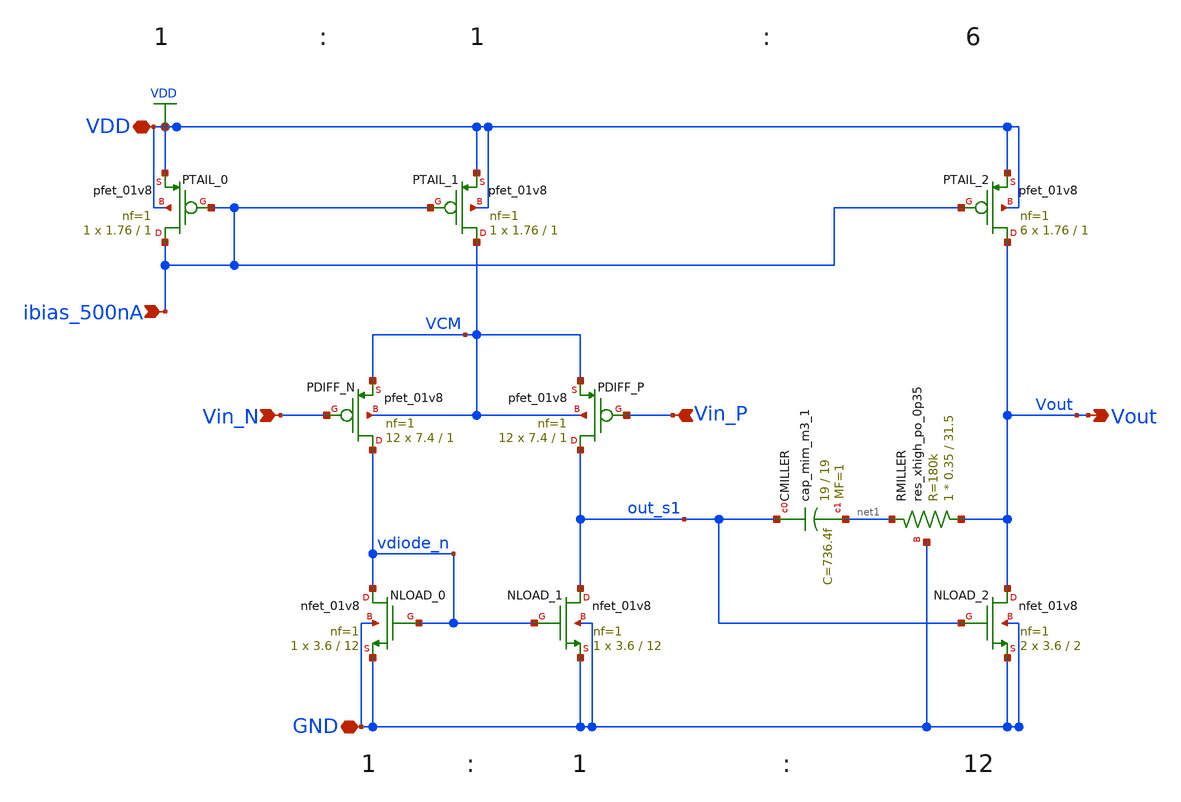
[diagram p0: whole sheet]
** sch_path: dfii/project_2stage_OTA/ota_2stage_transistor.sch
**.subckt ota_2stage_transistor VDD GND ibias_500nA Vin_N Vin_P Vout
*.iopin VDD
*.iopin GND
*.ipin ibias_500nA
*.ipin Vin_N
*.ipin Vin_P
*.opin Vout
XNLOAD_0 vdiode_n vdiode_n GND GND sky130_fd_pr__nfet_01v8 L=12 W=3.6 nf=1 ad='int((1 + 1)/2) * 3.6 / 1 * 0.29'
+ as='int((1 + 2)/2) * 3.6 / 1 * 0.29' pd='2*int((1 + 1)/2) * (3.6 / 1 + 0.29)' ps='2*int((1 + 2)/2) * (3.6 / 1 + 0.29)'
+ nrd='0.29 / 3.6 ' nrs='0.29 / 3.6 ' sa=0 sb=0 sd=0 mult=1 m=1
XNLOAD_1 out_s1 vdiode_n GND GND sky130_fd_pr__nfet_01v8 L=12 W=3.6 nf=1 ad='int((1 + 1)/2) * 3.6 / 1 * 0.29'
+ as='int((1 + 2)/2) * 3.6 / 1 * 0.29' pd='2*int((1 + 1)/2) * (3.6 / 1 + 0.29)' ps='2*int((1 + 2)/2) * (3.6 / 1 + 0.29)'
+ nrd='0.29 / 3.6 ' nrs='0.29 / 3.6 ' sa=0 sb=0 sd=0 mult=1 m=1
XNLOAD_2 Vout out_s1 GND GND sky130_fd_pr__nfet_01v8 L=2 W=3.6 nf=1 ad='int((1 + 1)/2) * 3.6 / 1 * 0.29'
+ as='int((1 + 2)/2) * 3.6 / 1 * 0.29' pd='2*int((1 + 1)/2) * (3.6 / 1 + 0.29)' ps='2*int((1 + 2)/2) * (3.6 / 1 + 0.29)'
+ nrd='0.29 / 3.6 ' nrs='0.29 / 3.6 ' sa=0 sb=0 sd=0 mult=2 m=2
XPDIFF_N vdiode_n Vin_N VCM VCM sky130_fd_pr__pfet_01v8 L=1 W=7.4 nf=1 ad='int((1 + 1)/2) * 7.4 / 1 * 0.29'
+ as='int((1 + 2)/2) * 7.4 / 1 * 0.29' pd='2*int((1 + 1)/2) * (7.4 / 1 + 0.29)' ps='2*int((1 + 2)/2) * (7.4 / 1 + 0.29)'
+ nrd='0.29 / 7.4 ' nrs='0.29 / 7.4 ' sa=0 sb=0 sd=0 mult=12 m=12
XPDIFF_P out_s1 Vin_P VCM VCM sky130_fd_pr__pfet_01v8 L=1 W=7.4 nf=1 ad='int((1 + 1)/2) * 7.4 / 1 * 0.29'
+ as='int((1 + 2)/2) * 7.4 / 1 * 0.29' pd='2*int((1 + 1)/2) * (7.4 / 1 + 0.29)' ps='2*int((1 + 2)/2) * (7.4 / 1 + 0.29)'
+ nrd='0.29 / 7.4 ' nrs='0.29 / 7.4 ' sa=0 sb=0 sd=0 mult=12 m=12
XPTAIL_1 VCM ibias_500nA VDD VDD sky130_fd_pr__pfet_01v8 L=1 W=1.76 nf=1 ad='int((1 + 1)/2) * 1.76 / 1 * 0.29'
+ as='int((1 + 2)/2) * 1.76 / 1 * 0.29' pd='2*int((1 + 1)/2) * (1.76 / 1 + 0.29)' ps='2*int((1 + 2)/2) * (1.76 / 1 + 0.29)'
+ nrd='0.29 / 1.76 ' nrs='0.29 / 1.76 ' sa=0 sb=0 sd=0 mult=1 m=1
XPTAIL_2 Vout ibias_500nA VDD VDD sky130_fd_pr__pfet_01v8 L=1 W=1.76 nf=1 ad='int((1 + 1)/2) * 1.76 / 1 * 0.29'
+ as='int((1 + 2)/2) * 1.76 / 1 * 0.29' pd='2*int((1 + 1)/2) * (1.76 / 1 + 0.29)' ps='2*int((1 + 2)/2) * (1.76 / 1 + 0.29)'
+ nrd='0.29 / 1.76 ' nrs='0.29 / 1.76 ' sa=0 sb=0 sd=0 mult=6 m=6
XPTAIL_0 ibias_500nA ibias_500nA VDD VDD sky130_fd_pr__pfet_01v8 L=1 W=1.76 nf=1 ad='int((1 + 1)/2) * 1.76 / 1 * 0.29'
+ as='int((1 + 2)/2) * 1.76 / 1 * 0.29' pd='2*int((1 + 1)/2) * (1.76 / 1 + 0.29)' ps='2*int((1 + 2)/2) * (1.76 / 1 + 0.29)'
+ nrd='0.29 / 1.76 ' nrs='0.29 / 1.76 ' sa=0 sb=0 sd=0 mult=1 m=1
XCMILLER out_s1 net1 sky130_fd_pr__cap_mim_m3_1 W=19 L=19 MF=1 m=1
XRMILLER Vout net1 GND sky130_fd_pr__res_xhigh_po_0p35 L=31.5 mult=1 m=1
**.ends
.GLOBAL VDD
.end
